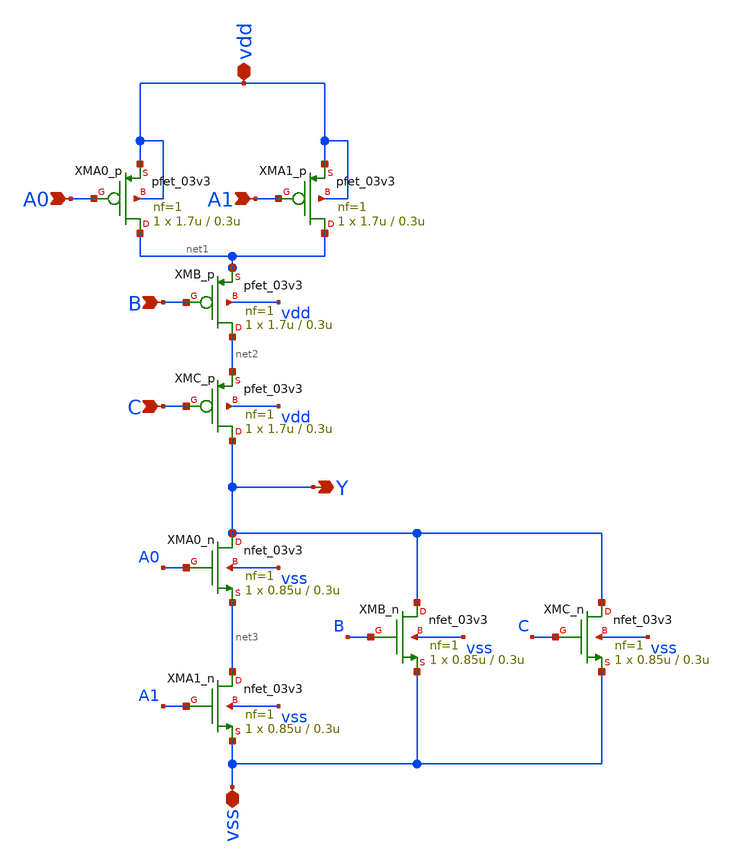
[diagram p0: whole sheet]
** sch_path: gf180mcu_osu_sc_gp9t3v3/xschem/gf180mcu_osu_sc_gp9t3v3__aoi211_1.sch
**.subckt gf180mcu_osu_sc_gp9t3v3__aoi211_1 Y A0 A1 B C vdd vss
*.opin Y
*.ipin A0
*.ipin A1
*.ipin B
*.ipin C
*.iopin vdd
*.iopin vss
XMA0_n Y A0 net3 vss nfet_03v3 L=0.3u W=0.85u nf=1 ad='int((nf+1)/2) * W/nf * 0.18u' as='int((nf+2)/2) * W/nf * 0.18u'
+ pd='2*int((nf+1)/2) * (W/nf + 0.18u)' ps='2*int((nf+2)/2) * (W/nf + 0.18u)' nrd='0.18u / W' nrs='0.18u / W'
+ sa=0 sb=0 sd=0 m=1
XMA1_n net3 A1 vss vss nfet_03v3 L=0.3u W=0.85u nf=1 ad='int((nf+1)/2) * W/nf * 0.18u' as='int((nf+2)/2) * W/nf * 0.18u'
+ pd='2*int((nf+1)/2) * (W/nf + 0.18u)' ps='2*int((nf+2)/2) * (W/nf + 0.18u)' nrd='0.18u / W' nrs='0.18u / W'
+ sa=0 sb=0 sd=0 m=1
XMB_n Y B vss vss nfet_03v3 L=0.3u W=0.85u nf=1 ad='int((nf+1)/2) * W/nf * 0.18u' as='int((nf+2)/2) * W/nf * 0.18u'
+ pd='2*int((nf+1)/2) * (W/nf + 0.18u)' ps='2*int((nf+2)/2) * (W/nf + 0.18u)' nrd='0.18u / W' nrs='0.18u / W'
+ sa=0 sb=0 sd=0 m=1
XMC_n Y C vss vss nfet_03v3 L=0.3u W=0.85u nf=1 ad='int((nf+1)/2) * W/nf * 0.18u' as='int((nf+2)/2) * W/nf * 0.18u'
+ pd='2*int((nf+1)/2) * (W/nf + 0.18u)' ps='2*int((nf+2)/2) * (W/nf + 0.18u)' nrd='0.18u / W' nrs='0.18u / W'
+ sa=0 sb=0 sd=0 m=1
XMA0_p net1 A0 vdd vdd pfet_03v3 L=0.3u W=1.7u nf=1 ad='int((nf+1)/2) * W/nf * 0.18u' as='int((nf+2)/2) * W/nf * 0.18u'
+ pd='2*int((nf+1)/2) * (W/nf + 0.18u)' ps='2*int((nf+2)/2) * (W/nf + 0.18u)' nrd='0.18u / W' nrs='0.18u / W'
+ sa=0 sb=0 sd=0 m=1
XMA1_p net1 A1 vdd vdd pfet_03v3 L=0.3u W=1.7u nf=1 ad='int((nf+1)/2) * W/nf * 0.18u' as='int((nf+2)/2) * W/nf * 0.18u'
+ pd='2*int((nf+1)/2) * (W/nf + 0.18u)' ps='2*int((nf+2)/2) * (W/nf + 0.18u)' nrd='0.18u / W' nrs='0.18u / W'
+ sa=0 sb=0 sd=0 m=1
XMB_p net2 B net1 vdd pfet_03v3 L=0.3u W=1.7u nf=1 ad='int((nf+1)/2) * W/nf * 0.18u' as='int((nf+2)/2) * W/nf * 0.18u'
+ pd='2*int((nf+1)/2) * (W/nf + 0.18u)' ps='2*int((nf+2)/2) * (W/nf + 0.18u)' nrd='0.18u / W' nrs='0.18u / W'
+ sa=0 sb=0 sd=0 m=1
XMC_p Y C net2 vdd pfet_03v3 L=0.3u W=1.7u nf=1 ad='int((nf+1)/2) * W/nf * 0.18u' as='int((nf+2)/2) * W/nf * 0.18u'
+ pd='2*int((nf+1)/2) * (W/nf + 0.18u)' ps='2*int((nf+2)/2) * (W/nf + 0.18u)' nrd='0.18u / W' nrs='0.18u / W'
+ sa=0 sb=0 sd=0 m=1
**.ends
.end
